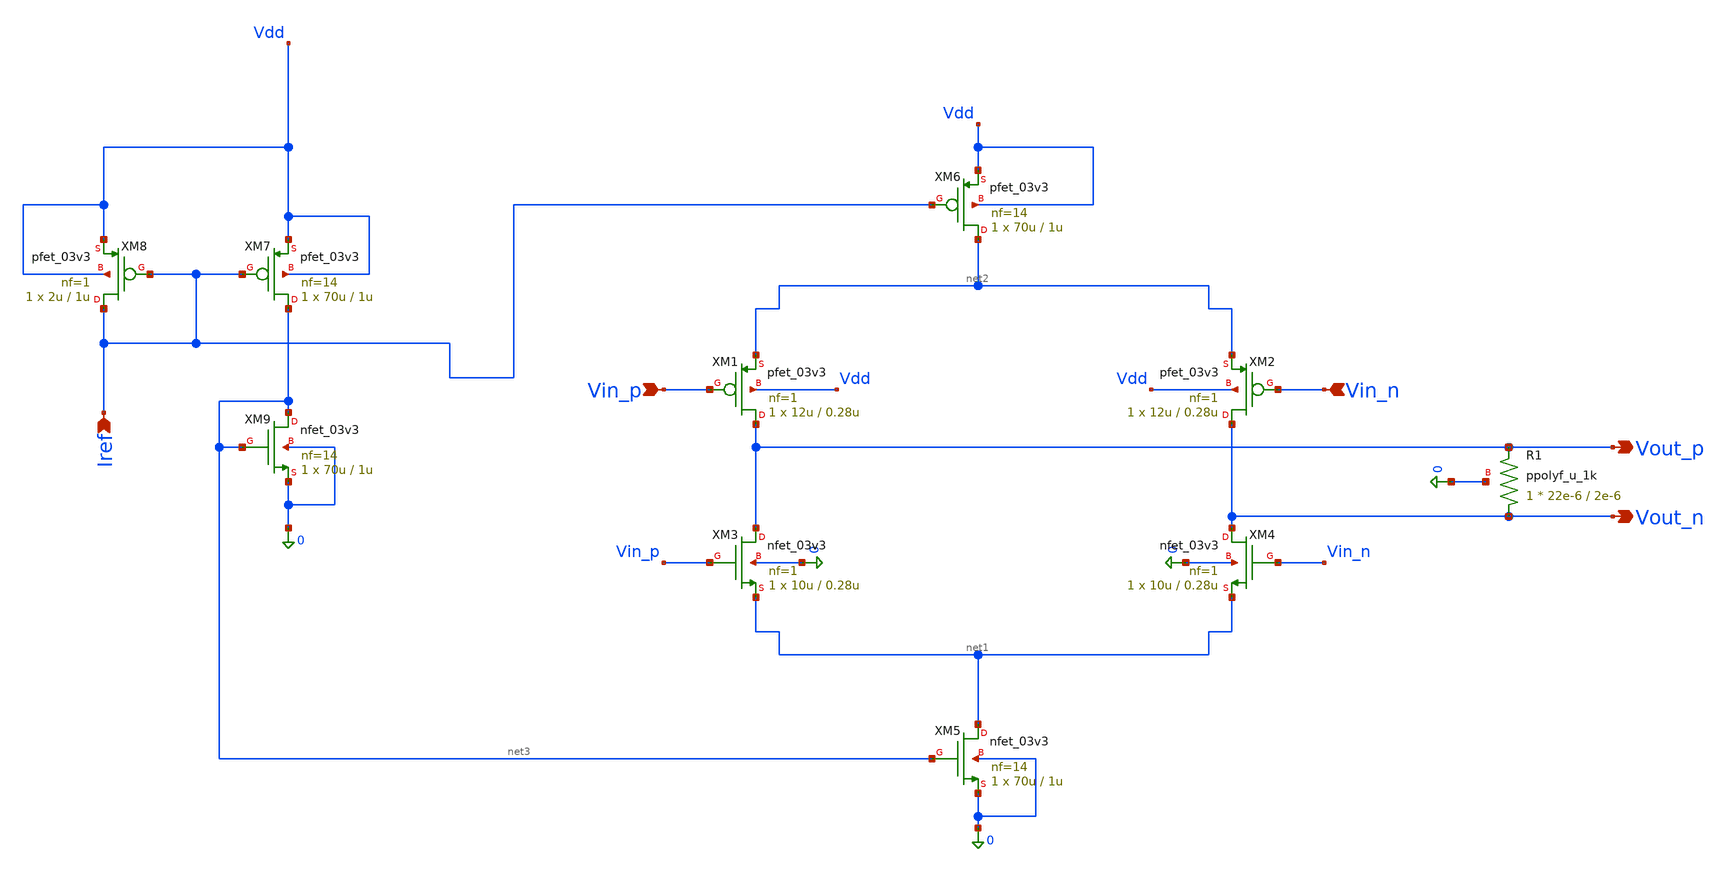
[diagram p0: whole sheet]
** sch_path: blocks/adc/lvds/lvds_v5.sch
**.subckt lvds_v5 Vin_n Vin_p Vout_p Vout_n Iref
*.ipin Vin_n
*.ipin Vin_p
*.opin Vout_p
*.opin Vout_n
*.ipin Iref
XR1 Vout_n Vout_p 0 ppolyf_u_1k r_width=22e-6 r_length=2e-6 m=1
XM1 Vout_p Vin_p net2 Vdd pfet_03v3 L=0.28u W=12u nf=1 ad='int((nf+1)/2) * W/nf * 0.18u' as='int((nf+2)/2) * W/nf * 0.18u'
+ pd='2*int((nf+1)/2) * (W/nf + 0.18u)' ps='2*int((nf+2)/2) * (W/nf + 0.18u)' nrd='0.18u / W' nrs='0.18u / W'
+ sa=0 sb=0 sd=0 m=1
XM2 Vout_n Vin_n net2 Vdd pfet_03v3 L=0.28u W=12u nf=1 ad='int((nf+1)/2) * W/nf * 0.18u' as='int((nf+2)/2) * W/nf * 0.18u'
+ pd='2*int((nf+1)/2) * (W/nf + 0.18u)' ps='2*int((nf+2)/2) * (W/nf + 0.18u)' nrd='0.18u / W' nrs='0.18u / W'
+ sa=0 sb=0 sd=0 m=1
XM3 Vout_p Vin_p net1 0 nfet_03v3 L=0.28u W=10u nf=1 ad='int((nf+1)/2) * W/nf * 0.18u' as='int((nf+2)/2) * W/nf * 0.18u'
+ pd='2*int((nf+1)/2) * (W/nf + 0.18u)' ps='2*int((nf+2)/2) * (W/nf + 0.18u)' nrd='0.18u / W' nrs='0.18u / W'
+ sa=0 sb=0 sd=0 m=1
XM4 Vout_n Vin_n net1 0 nfet_03v3 L=0.28u W=10u nf=1 ad='int((nf+1)/2) * W/nf * 0.18u' as='int((nf+2)/2) * W/nf * 0.18u'
+ pd='2*int((nf+1)/2) * (W/nf + 0.18u)' ps='2*int((nf+2)/2) * (W/nf + 0.18u)' nrd='0.18u / W' nrs='0.18u / W'
+ sa=0 sb=0 sd=0 m=1
XM5 net1 net3 0 0 nfet_03v3 L=1u W=70u nf=14 ad='int((nf+1)/2) * W/nf * 0.18u' as='int((nf+2)/2) * W/nf * 0.18u'
+ pd='2*int((nf+1)/2) * (W/nf + 0.18u)' ps='2*int((nf+2)/2) * (W/nf + 0.18u)' nrd='0.18u / W' nrs='0.18u / W'
+ sa=0 sb=0 sd=0 m=1
XM6 net2 Iref Vdd Vdd pfet_03v3 L=1u W=70u nf=14 ad='int((nf+1)/2) * W/nf * 0.18u' as='int((nf+2)/2) * W/nf * 0.18u'
+ pd='2*int((nf+1)/2) * (W/nf + 0.18u)' ps='2*int((nf+2)/2) * (W/nf + 0.18u)' nrd='0.18u / W' nrs='0.18u / W'
+ sa=0 sb=0 sd=0 m=1
XM7 net3 Iref Vdd Vdd pfet_03v3 L=1u W=70u nf=14 ad='int((nf+1)/2) * W/nf * 0.18u' as='int((nf+2)/2) * W/nf * 0.18u'
+ pd='2*int((nf+1)/2) * (W/nf + 0.18u)' ps='2*int((nf+2)/2) * (W/nf + 0.18u)' nrd='0.18u / W' nrs='0.18u / W'
+ sa=0 sb=0 sd=0 m=1
XM8 Iref Iref Vdd Vdd pfet_03v3 L=1u W=2u nf=1 ad='int((nf+1)/2) * W/nf * 0.18u' as='int((nf+2)/2) * W/nf * 0.18u'
+ pd='2*int((nf+1)/2) * (W/nf + 0.18u)' ps='2*int((nf+2)/2) * (W/nf + 0.18u)' nrd='0.18u / W' nrs='0.18u / W'
+ sa=0 sb=0 sd=0 m=1
XM9 net3 net3 0 0 nfet_03v3 L=1u W=70u nf=14 ad='int((nf+1)/2) * W/nf * 0.18u' as='int((nf+2)/2) * W/nf * 0.18u'
+ pd='2*int((nf+1)/2) * (W/nf + 0.18u)' ps='2*int((nf+2)/2) * (W/nf + 0.18u)' nrd='0.18u / W' nrs='0.18u / W'
+ sa=0 sb=0 sd=0 m=1
**.ends
.end
